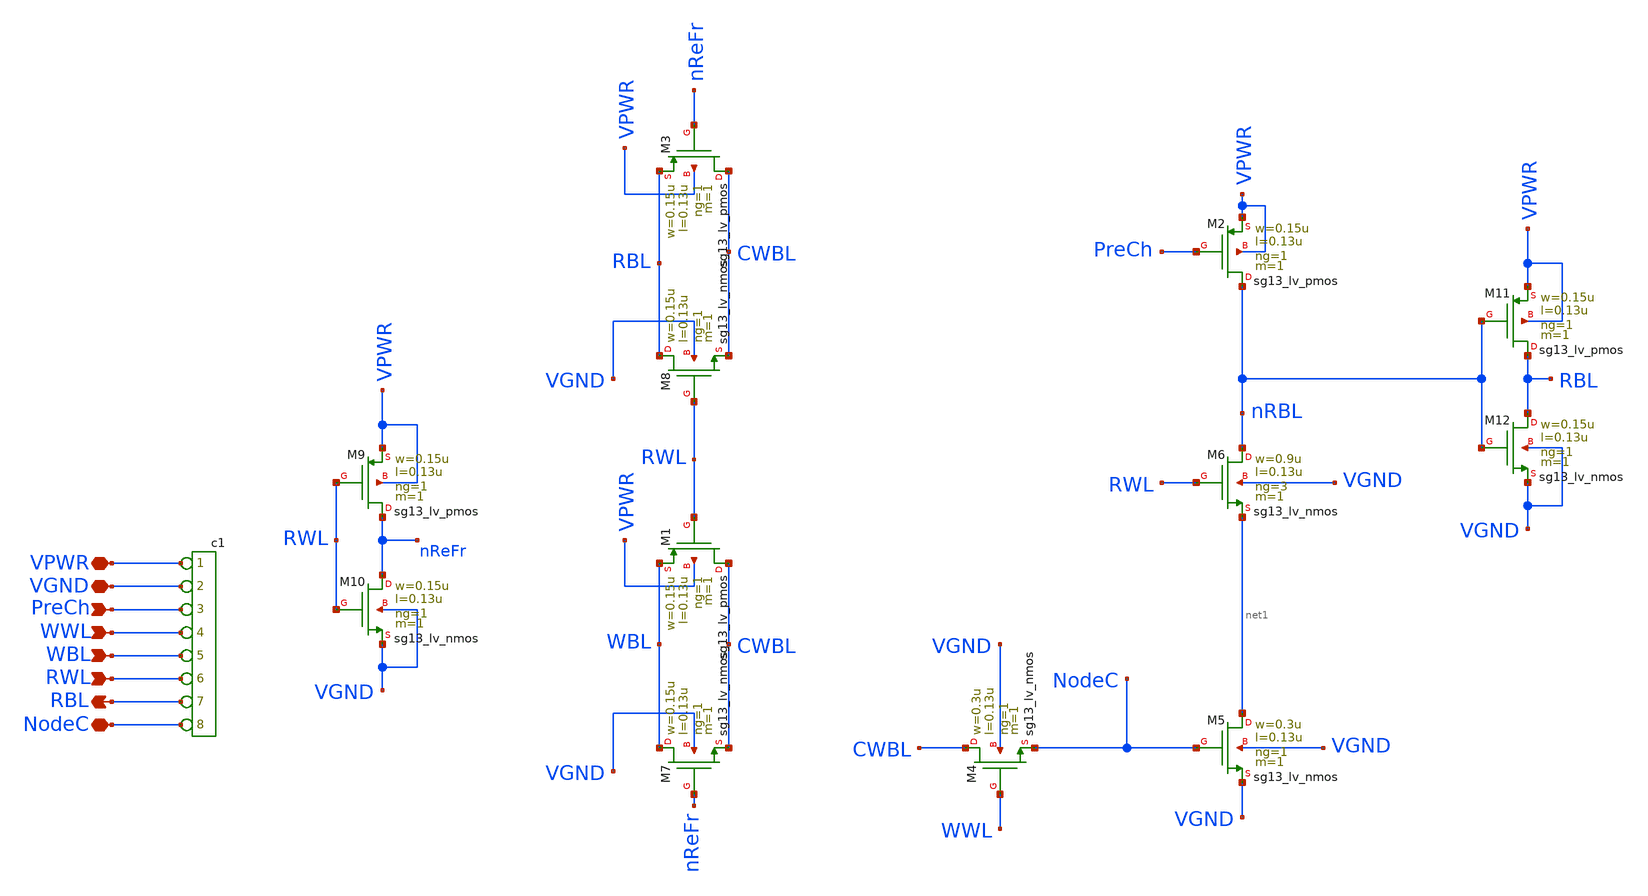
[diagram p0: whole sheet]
** sch_path: macros/heichips26_analog_project/macros/dramcell_2_0/schematic/xschem/dramcell_2_0_c.sch
**.subckt dramcell_2_0_c RBL WWL WBL RWL VGND NodeC VPWR PreCh
*.opin RBL
*.ipin WWL
*.ipin WBL
*.ipin RWL
*.iopin VGND
*.iopin NodeC
*.iopin VPWR
*.ipin PreCh
XM4 CWBL WWL NodeC VGND sg13_lv_nmos w=0.3u l=0.13u ng=1 m=1 mm_ok=1
XM5 net1 NodeC VGND VGND sg13_lv_nmos w=0.3u l=0.13u ng=1 m=1 mm_ok=1
XM6 nRBL RWL net1 VGND sg13_lv_nmos w=0.9u l=0.13u ng=3 m=1 mm_ok=1
XM2 nRBL PreCh VPWR VPWR sg13_lv_pmos w=0.15u l=0.13u ng=1 m=1 mm_ok=1
XM1 CWBL RWL WBL VPWR sg13_lv_pmos w=0.15u l=0.13u ng=1 m=1 mm_ok=1
XM7 WBL nReFr CWBL VGND sg13_lv_nmos w=0.15u l=0.13u ng=1 m=1 mm_ok=1
XM3 CWBL nReFr RBL VPWR sg13_lv_pmos w=0.15u l=0.13u ng=1 m=1 mm_ok=1
XM8 RBL RWL CWBL VGND sg13_lv_nmos w=0.15u l=0.13u ng=1 m=1 mm_ok=1
XM9 nReFr RWL VPWR VPWR sg13_lv_pmos w=0.15u l=0.13u ng=1 m=1 mm_ok=1
XM10 nReFr RWL VGND VGND sg13_lv_nmos w=0.15u l=0.13u ng=1 m=1 mm_ok=1
XM11 RBL nRBL VPWR VPWR sg13_lv_pmos w=0.15u l=0.13u ng=1 m=1 mm_ok=1
XM12 RBL nRBL VGND VGND sg13_lv_nmos w=0.15u l=0.13u ng=1 m=1 mm_ok=1
*connector(8,1) ?1 VPWR ?1 VGND ?1 PreCh ?1 WWL ?1 WBL ?1 RWL ?1 RBL ?1 NodeC
**.ends
.end
